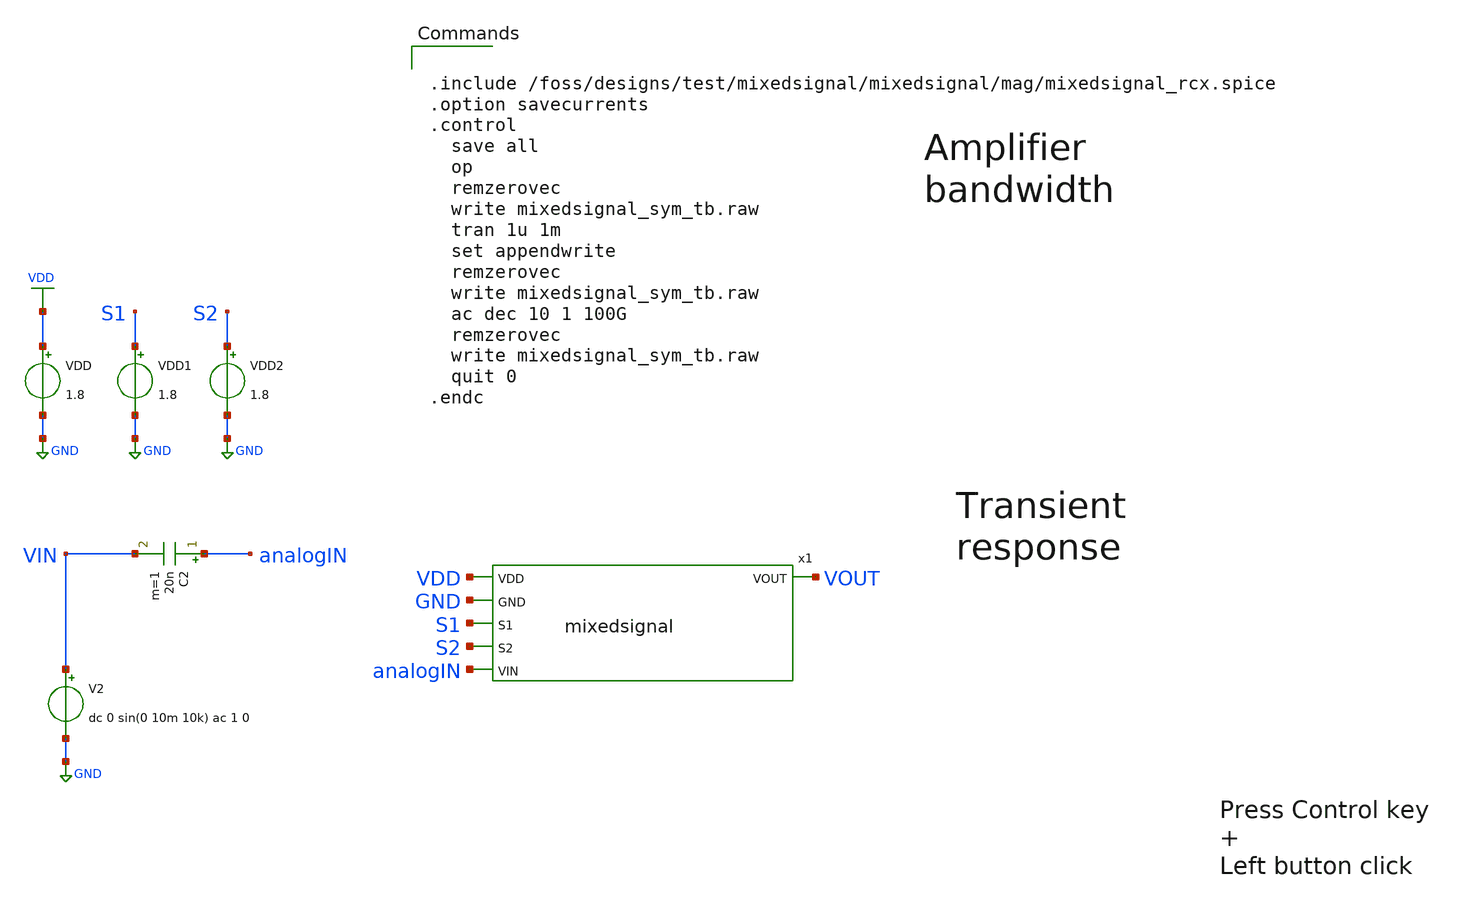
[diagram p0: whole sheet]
** sch_path: xschem/mixedsignal_post-layout_tb.sch
**.subckt mixedsignal_post-layout_tb
x1 VDD GND S1 S2 analogIN VOUT mixedsignal
VDD VDD GND 1.8
C2 analogIN VIN 20n m=1
V2 VIN GND dc 0 sin(0 10m 10k) ac 1 0
VDD2 S2 GND 1.8
VDD1 S1 GND 1.8
**** begin user architecture code

** opencircuitdesign pdks install
.lib $::SKYWATER_MODELS/sky130.lib.spice tt




.include /foss/designs/test/mixedsignal/mixedsignal/mag/mixedsignal_rcx.spice
.option savecurrents
.control
  save all
  op
  remzerovec
  write mixedsignal_sym_tb.raw
  tran 1u 1m
  set appendwrite
  remzerovec
  write mixedsignal_sym_tb.raw
  ac dec 10 1 100G
  remzerovec
  write mixedsignal_sym_tb.raw
  quit 0
.endc


**** end user architecture code
**.ends

* expanding   symbol:  mixedsignal.sym # of pins=6
** sym_path: xschem/mixedsignal.sym
** sch_path: xschem/mixedsignal.sch
.subckt mixedsignal VDD GND S1 S2 VIN VOUT
*.opin VOUT
*.ipin VIN
*.ipin S1
*.ipin S2
*.ipin VDD
*.ipin GND
R1 VOUT mux_in 300k m=1
XM3 VOUT mux_in VDD VDD sky130_fd_pr__pfet_01v8 L=0.5 W=4 nf=5 ad='int((nf+1)/2) * W/nf * 0.29' as='int((nf+2)/2) * W/nf * 0.29'
+ pd='2*int((nf+1)/2) * (W/nf + 0.29)' ps='2*int((nf+2)/2) * (W/nf + 0.29)' nrd='0.29 / W' nrs='0.29 / W'
+ sa=0 sb=0 sd=0 mult=1 m=1
XM4 VOUT mux_in GND GND sky130_fd_pr__nfet_01v8 L=0.5 W=4 nf=5 ad='int((nf+1)/2) * W/nf * 0.29' as='int((nf+2)/2) * W/nf * 0.29'
+ pd='2*int((nf+1)/2) * (W/nf + 0.29)' ps='2*int((nf+2)/2) * (W/nf + 0.29)' nrd='0.29 / W' nrs='0.29 / W'
+ sa=0 sb=0 sd=0 mult=1 m=1
R7 VOUT net3 100k m=1
x1 S1 S2 VDD GND net4 net1 mux_in net2 net3 4-to-1_analog_MUX
R8 VOUT net2 30k m=1
R9 mux_in VIN 3k m=1
* noconn VOUT
* noconn #net4
R2 VOUT net1 3k m=1
.ends


* expanding   symbol:  4-to-1_analog_MUX.sym # of pins=9
** sym_path: xschem/4-to-1_analog_MUX.sym
** sch_path: xschem/4-to-1_analog_MUX.sch
.subckt 4-to-1_analog_MUX S1 S2 VDD GND I1 I2 OUT I3 I4
*.ipin I1
*.ipin I2
*.ipin I3
*.ipin I4
*.opin OUT
*.ipin S1
*.ipin S2
*.ipin VDD
*.ipin GND
x1 S1 S1bar GND VDD Inverter
x2 S2 S2bar GND VDD Inverter
XM9 net1 S2 OUT VDD sky130_fd_pr__pfet_01v8 L=0.5 W=1 nf=1 ad='int((nf+1)/2) * W/nf * 0.29' as='int((nf+2)/2) * W/nf * 0.29'
+ pd='2*int((nf+1)/2) * (W/nf + 0.29)' ps='2*int((nf+2)/2) * (W/nf + 0.29)' nrd='0.29 / W' nrs='0.29 / W'
+ sa=0 sb=0 sd=0 mult=1 m=1
XM1 I1 S1 net1 VDD sky130_fd_pr__pfet_01v8 L=0.5 W=1 nf=1 ad='int((nf+1)/2) * W/nf * 0.29' as='int((nf+2)/2) * W/nf * 0.29'
+ pd='2*int((nf+1)/2) * (W/nf + 0.29)' ps='2*int((nf+2)/2) * (W/nf + 0.29)' nrd='0.29 / W' nrs='0.29 / W'
+ sa=0 sb=0 sd=0 mult=1 m=1
XM2 I3 S1bar net1 VDD sky130_fd_pr__pfet_01v8 L=0.5 W=1 nf=1 ad='int((nf+1)/2) * W/nf * 0.29' as='int((nf+2)/2) * W/nf * 0.29'
+ pd='2*int((nf+1)/2) * (W/nf + 0.29)' ps='2*int((nf+2)/2) * (W/nf + 0.29)' nrd='0.29 / W' nrs='0.29 / W'
+ sa=0 sb=0 sd=0 mult=1 m=1
XM5 I2 S1 net2 VDD sky130_fd_pr__pfet_01v8 L=0.5 W=1 nf=1 ad='int((nf+1)/2) * W/nf * 0.29' as='int((nf+2)/2) * W/nf * 0.29'
+ pd='2*int((nf+1)/2) * (W/nf + 0.29)' ps='2*int((nf+2)/2) * (W/nf + 0.29)' nrd='0.29 / W' nrs='0.29 / W'
+ sa=0 sb=0 sd=0 mult=1 m=1
XM7 I4 S1bar net2 VDD sky130_fd_pr__pfet_01v8 L=0.5 W=1 nf=1 ad='int((nf+1)/2) * W/nf * 0.29' as='int((nf+2)/2) * W/nf * 0.29'
+ pd='2*int((nf+1)/2) * (W/nf + 0.29)' ps='2*int((nf+2)/2) * (W/nf + 0.29)' nrd='0.29 / W' nrs='0.29 / W'
+ sa=0 sb=0 sd=0 mult=1 m=1
XM11 net2 S2bar OUT VDD sky130_fd_pr__pfet_01v8 L=0.5 W=1 nf=1 ad='int((nf+1)/2) * W/nf * 0.29' as='int((nf+2)/2) * W/nf * 0.29'
+ pd='2*int((nf+1)/2) * (W/nf + 0.29)' ps='2*int((nf+2)/2) * (W/nf + 0.29)' nrd='0.29 / W' nrs='0.29 / W'
+ sa=0 sb=0 sd=0 mult=1 m=1
XM3 I1 S1bar net1 GND sky130_fd_pr__nfet_01v8 L=1 W=1 nf=1 ad='int((nf+1)/2) * W/nf * 0.29' as='int((nf+2)/2) * W/nf * 0.29'
+ pd='2*int((nf+1)/2) * (W/nf + 0.29)' ps='2*int((nf+2)/2) * (W/nf + 0.29)' nrd='0.29 / W' nrs='0.29 / W'
+ sa=0 sb=0 sd=0 mult=1 m=1
XM4 I3 S1 net1 GND sky130_fd_pr__nfet_01v8 L=1 W=1 nf=1 ad='int((nf+1)/2) * W/nf * 0.29' as='int((nf+2)/2) * W/nf * 0.29'
+ pd='2*int((nf+1)/2) * (W/nf + 0.29)' ps='2*int((nf+2)/2) * (W/nf + 0.29)' nrd='0.29 / W' nrs='0.29 / W'
+ sa=0 sb=0 sd=0 mult=1 m=1
XM10 net1 S2bar OUT GND sky130_fd_pr__nfet_01v8 L=1 W=1 nf=1 ad='int((nf+1)/2) * W/nf * 0.29' as='int((nf+2)/2) * W/nf * 0.29'
+ pd='2*int((nf+1)/2) * (W/nf + 0.29)' ps='2*int((nf+2)/2) * (W/nf + 0.29)' nrd='0.29 / W' nrs='0.29 / W'
+ sa=0 sb=0 sd=0 mult=1 m=1
XM6 I2 S1bar net2 GND sky130_fd_pr__nfet_01v8 L=1 W=1 nf=1 ad='int((nf+1)/2) * W/nf * 0.29' as='int((nf+2)/2) * W/nf * 0.29'
+ pd='2*int((nf+1)/2) * (W/nf + 0.29)' ps='2*int((nf+2)/2) * (W/nf + 0.29)' nrd='0.29 / W' nrs='0.29 / W'
+ sa=0 sb=0 sd=0 mult=1 m=1
XM8 I4 S1 net2 GND sky130_fd_pr__nfet_01v8 L=1 W=1 nf=1 ad='int((nf+1)/2) * W/nf * 0.29' as='int((nf+2)/2) * W/nf * 0.29'
+ pd='2*int((nf+1)/2) * (W/nf + 0.29)' ps='2*int((nf+2)/2) * (W/nf + 0.29)' nrd='0.29 / W' nrs='0.29 / W'
+ sa=0 sb=0 sd=0 mult=1 m=1
XM12 net2 S2 OUT GND sky130_fd_pr__nfet_01v8 L=1 W=1 nf=1 ad='int((nf+1)/2) * W/nf * 0.29' as='int((nf+2)/2) * W/nf * 0.29'
+ pd='2*int((nf+1)/2) * (W/nf + 0.29)' ps='2*int((nf+2)/2) * (W/nf + 0.29)' nrd='0.29 / W' nrs='0.29 / W'
+ sa=0 sb=0 sd=0 mult=1 m=1
.ends


* expanding   symbol:  Inverter.sym # of pins=4
** sym_path: xschem/Inverter.sym
** sch_path: xschem/Inverter.sch
.subckt Inverter Vin Vout GND VDD
*.opin Vout
*.ipin Vin
*.ipin VDD
*.ipin GND
XM1 Vout Vin VDD VDD sky130_fd_pr__pfet_01v8 L=0.5 W=1 nf=1 ad='int((nf+1)/2) * W/nf * 0.29' as='int((nf+2)/2) * W/nf * 0.29'
+ pd='2*int((nf+1)/2) * (W/nf + 0.29)' ps='2*int((nf+2)/2) * (W/nf + 0.29)' nrd='0.29 / W' nrs='0.29 / W'
+ sa=0 sb=0 sd=0 mult=1 m=1
XM2 Vout Vin GND GND sky130_fd_pr__nfet_01v8 L=1 W=1 nf=1 ad='int((nf+1)/2) * W/nf * 0.29' as='int((nf+2)/2) * W/nf * 0.29'
+ pd='2*int((nf+1)/2) * (W/nf + 0.29)' ps='2*int((nf+2)/2) * (W/nf + 0.29)' nrd='0.29 / W' nrs='0.29 / W'
+ sa=0 sb=0 sd=0 mult=1 m=1
.ends

.GLOBAL GND
.GLOBAL VDD
.end
